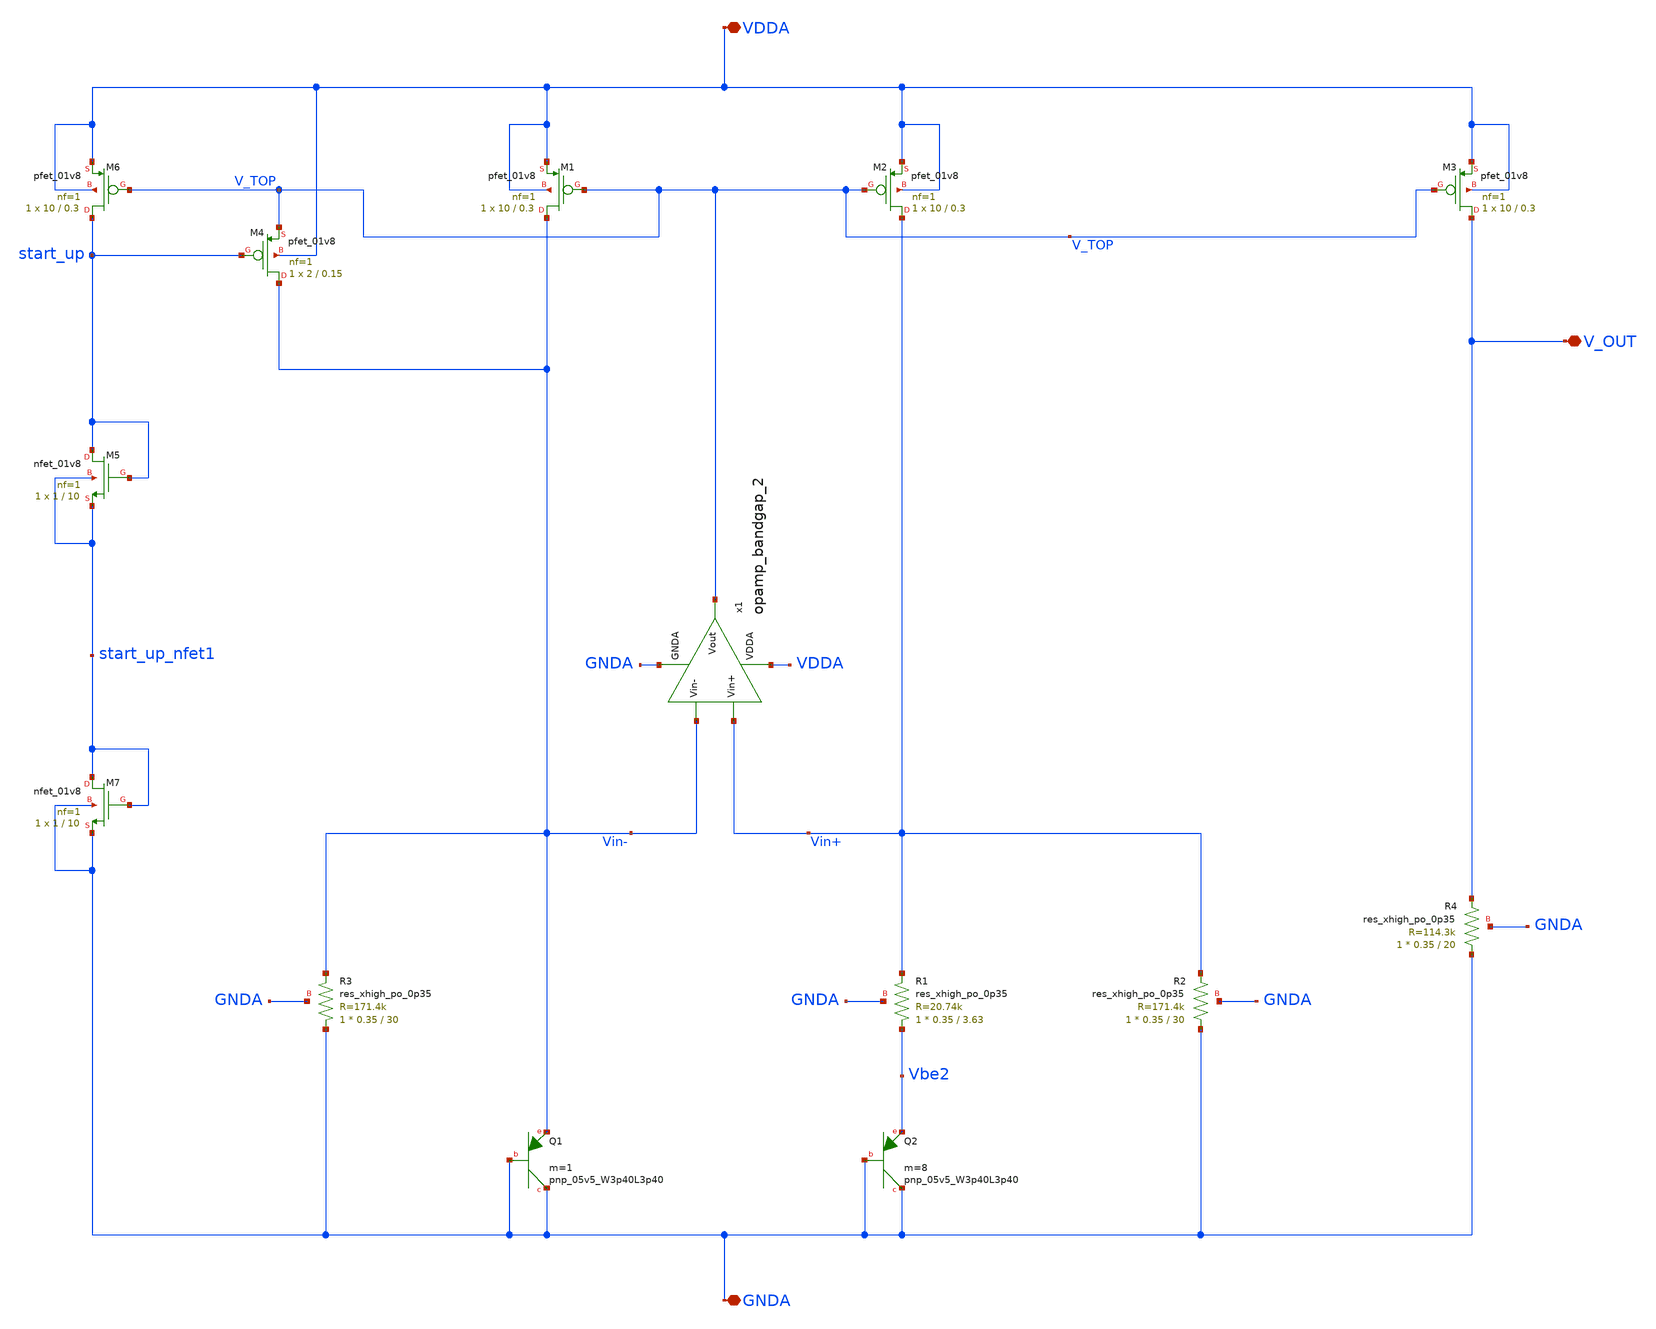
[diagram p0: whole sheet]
** sch_path: projects/bandgapref/xschem_ngspice/new_files/low_voltage_BGR_2.sch
**.subckt low_voltage_BGR_2 VDDA GNDA V_OUT
*.iopin VDDA
*.iopin GNDA
*.iopin V_OUT
XQ1 GNDA GNDA Vin- sky130_fd_pr__pnp_05v5_W3p40L3p40 m=1
XQ2 GNDA GNDA Vbe2 sky130_fd_pr__pnp_05v5_W3p40L3p40 m=8
XM1 Vin- V_TOP VDDA VDDA sky130_fd_pr__pfet_01v8 L=0.3 W=10 nf=1 ad='int((nf+1)/2) * W/nf * 0.29' as='int((nf+2)/2) * W/nf * 0.29'
+ pd='2*int((nf+1)/2) * (W/nf + 0.29)' ps='2*int((nf+2)/2) * (W/nf + 0.29)' nrd='0.29 / W' nrs='0.29 / W'
+ sa=0 sb=0 sd=0 mult=1 m=1
XM2 Vin+ V_TOP VDDA VDDA sky130_fd_pr__pfet_01v8 L=0.3 W=10 nf=1 ad='int((nf+1)/2) * W/nf * 0.29' as='int((nf+2)/2) * W/nf * 0.29'
+ pd='2*int((nf+1)/2) * (W/nf + 0.29)' ps='2*int((nf+2)/2) * (W/nf + 0.29)' nrd='0.29 / W' nrs='0.29 / W'
+ sa=0 sb=0 sd=0 mult=1 m=1
XM3 V_OUT V_TOP VDDA VDDA sky130_fd_pr__pfet_01v8 L=0.3 W=10 nf=1 ad='int((nf+1)/2) * W/nf * 0.29' as='int((nf+2)/2) * W/nf * 0.29'
+ pd='2*int((nf+1)/2) * (W/nf + 0.29)' ps='2*int((nf+2)/2) * (W/nf + 0.29)' nrd='0.29 / W' nrs='0.29 / W'
+ sa=0 sb=0 sd=0 mult=1 m=1
XR1 Vbe2 Vin+ GNDA sky130_fd_pr__res_xhigh_po_0p35 L=3.63 mult=1 m=1
XR2 GNDA Vin+ GNDA sky130_fd_pr__res_xhigh_po_0p35 L=30 mult=1 m=1
XR3 GNDA Vin- GNDA sky130_fd_pr__res_xhigh_po_0p35 L=30 mult=1 m=1
XR4 GNDA V_OUT GNDA sky130_fd_pr__res_xhigh_po_0p35 L=20 mult=1 m=1
XM5 start_up start_up start_up_nfet1 start_up_nfet1 sky130_fd_pr__nfet_01v8 L=10 W=1 nf=1 ad='int((nf+1)/2) * W/nf * 0.29'
+ as='int((nf+2)/2) * W/nf * 0.29' pd='2*int((nf+1)/2) * (W/nf + 0.29)' ps='2*int((nf+2)/2) * (W/nf + 0.29)'
+ nrd='0.29 / W' nrs='0.29 / W' sa=0 sb=0 sd=0 mult=1 m=1
XM6 start_up V_TOP VDDA VDDA sky130_fd_pr__pfet_01v8 L=0.3 W=10 nf=1 ad='int((nf+1)/2) * W/nf * 0.29'
+ as='int((nf+2)/2) * W/nf * 0.29' pd='2*int((nf+1)/2) * (W/nf + 0.29)' ps='2*int((nf+2)/2) * (W/nf + 0.29)'
+ nrd='0.29 / W' nrs='0.29 / W' sa=0 sb=0 sd=0 mult=1 m=1
XM4 Vin- start_up V_TOP VDDA sky130_fd_pr__pfet_01v8 L=0.15 W=2 nf=1 ad='int((nf+1)/2) * W/nf * 0.29'
+ as='int((nf+2)/2) * W/nf * 0.29' pd='2*int((nf+1)/2) * (W/nf + 0.29)' ps='2*int((nf+2)/2) * (W/nf + 0.29)'
+ nrd='0.29 / W' nrs='0.29 / W' sa=0 sb=0 sd=0 mult=1 m=1
x1 VDDA V_TOP Vin- Vin+ GNDA opamp_bandgap_2
XM7 start_up_nfet1 start_up_nfet1 GNDA GNDA sky130_fd_pr__nfet_01v8 L=10 W=1 nf=1 ad='int((nf+1)/2) * W/nf * 0.29'
+ as='int((nf+2)/2) * W/nf * 0.29' pd='2*int((nf+1)/2) * (W/nf + 0.29)' ps='2*int((nf+2)/2) * (W/nf + 0.29)'
+ nrd='0.29 / W' nrs='0.29 / W' sa=0 sb=0 sd=0 mult=1 m=1
**.ends

* expanding   symbol:  opamp_bandgap_2.sym # of pins=5
** sym_path: projects/bandgapref/xschem_ngspice/new_files/opamp_bandgap_2.sym
** sch_path: projects/bandgapref/xschem_ngspice/new_files/opamp_bandgap_2.sch
.subckt opamp_bandgap_2 VDDA Vout Vin- Vin+ GNDA
*.ipin Vin+
*.opin Vout
*.ipin Vin-
*.ipin GNDA
*.ipin VDDA
XM1 V_p VDDA GNDA GNDA sky130_fd_pr__nfet_01v8 L=10 W=5 nf=1 ad='int((nf+1)/2) * W/nf * 0.29' as='int((nf+2)/2) * W/nf * 0.29'
+ pd='2*int((nf+1)/2) * (W/nf + 0.29)' ps='2*int((nf+2)/2) * (W/nf + 0.29)' nrd='0.29 / W' nrs='0.29 / W'
+ sa=0 sb=0 sd=0 mult=1 m=1
XM2 V_mirror Vin- V_p GNDA sky130_fd_pr__nfet_01v8 L=0.2 W=5 nf=1 ad='int((nf+1)/2) * W/nf * 0.29' as='int((nf+2)/2) * W/nf * 0.29'
+ pd='2*int((nf+1)/2) * (W/nf + 0.29)' ps='2*int((nf+2)/2) * (W/nf + 0.29)' nrd='0.29 / W' nrs='0.29 / W'
+ sa=0 sb=0 sd=0 mult=1 m=1
XM3 1st_Vout Vin+ V_p GNDA sky130_fd_pr__nfet_01v8 L=0.2 W=5 nf=1 ad='int((nf+1)/2) * W/nf * 0.29' as='int((nf+2)/2) * W/nf * 0.29'
+ pd='2*int((nf+1)/2) * (W/nf + 0.29)' ps='2*int((nf+2)/2) * (W/nf + 0.29)' nrd='0.29 / W' nrs='0.29 / W'
+ sa=0 sb=0 sd=0 mult=1 m=1
XM5 V_mirror V_mirror VDDA VDDA sky130_fd_pr__pfet_01v8 L=0.2 W=10 nf=2 ad='int((nf+1)/2) * W/nf * 0.29'
+ as='int((nf+2)/2) * W/nf * 0.29' pd='2*int((nf+1)/2) * (W/nf + 0.29)' ps='2*int((nf+2)/2) * (W/nf + 0.29)'
+ nrd='0.29 / W' nrs='0.29 / W' sa=0 sb=0 sd=0 mult=1 m=1
XM6 1st_Vout V_mirror VDDA VDDA sky130_fd_pr__pfet_01v8 L=0.2 W=10 nf=2 ad='int((nf+1)/2) * W/nf * 0.29'
+ as='int((nf+2)/2) * W/nf * 0.29' pd='2*int((nf+1)/2) * (W/nf + 0.29)' ps='2*int((nf+2)/2) * (W/nf + 0.29)'
+ nrd='0.29 / W' nrs='0.29 / W' sa=0 sb=0 sd=0 mult=1 m=1
XM4 Vout VDDA GNDA GNDA sky130_fd_pr__nfet_01v8 L=10 W=5 nf=1 ad='int((nf+1)/2) * W/nf * 0.29' as='int((nf+2)/2) * W/nf * 0.29'
+ pd='2*int((nf+1)/2) * (W/nf + 0.29)' ps='2*int((nf+2)/2) * (W/nf + 0.29)' nrd='0.29 / W' nrs='0.29 / W'
+ sa=0 sb=0 sd=0 mult=1 m=1
XM7 Vout 1st_Vout VDDA VDDA sky130_fd_pr__pfet_01v8 L=0.2 W=10 nf=2 ad='int((nf+1)/2) * W/nf * 0.29'
+ as='int((nf+2)/2) * W/nf * 0.29' pd='2*int((nf+1)/2) * (W/nf + 0.29)' ps='2*int((nf+2)/2) * (W/nf + 0.29)'
+ nrd='0.29 / W' nrs='0.29 / W' sa=0 sb=0 sd=0 mult=1 m=1
.ends

.end
